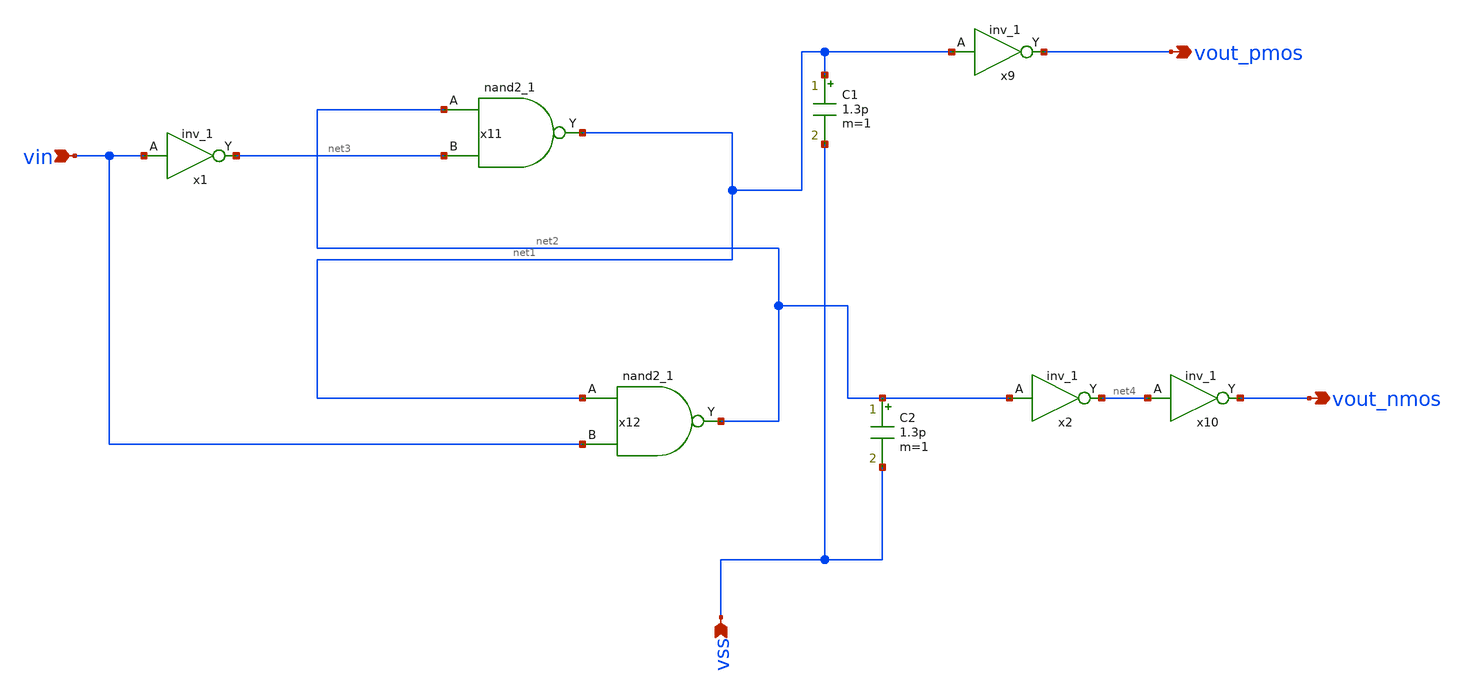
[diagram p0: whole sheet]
** sch_path: designs/libs/core_analog/Deadtime_Driver/op_Deadtime_Driver.sch
**.subckt op_Deadtime_Driver vin vss vout_pmos vout_nmos
*.ipin vin
*.ipin vss
*.opin vout_pmos
*.opin vout_nmos
C1 net1 vss 1.3p m=1
C2 net2 vss 1.3p m=1
x1 vin VSSd VDDd VSSd VDDd net3 gf180mcu_fd_sc_mcu9t5v0__inv_1
x2 net2 VSSd VDDd VSSd VDDd net4 gf180mcu_fd_sc_mcu9t5v0__inv_1
x9 net1 VSSd VDDd VSSd VDDd vout_pmos gf180mcu_fd_sc_mcu9t5v0__inv_1
x10 net4 VSSd VDDd VSSd VDDd vout_nmos gf180mcu_fd_sc_mcu9t5v0__inv_1
x11 net2 net3 VSSd VDDd VSSd VDDd net1 gf180mcu_fd_sc_mcu9t5v0__nand2_1
x12 net1 vin VSSd VDDd VSSd VDDd net2 gf180mcu_fd_sc_mcu9t5v0__nand2_1
**** begin user architecture code

.include $::180MCU_MODELS/design.ngspice
.include /foss/pdks/gf180mcuD/libs.ref/gf180mcu_fd_sc_mcu9t5v0/spice/gf180mcu_fd_sc_mcu9t5v0.spice
.lib $::180MCU_MODELS/sm141064.ngspice typical




.global VDDd VSSd
.control
save all
**Frequency & time settings
let fsig = 900k
let tper=1/fsig
let tfr = 0.01*tper
let ton = 0.5*tper-2*tfr

let tstop = 4 * tper
let tstep = 0.001*tper


**voltages
alter @Vin[PULSE] = [ 0 2.3 0 $&tfr $&tfr $&ton $&tper 3 ]
alter @Vin[DC] = 0
*alter @Vin[SIN] = [ 1.7 1.5 $&fsig 0 0 ]

**simulation
OP
*show all > op.log
show all

tran $&tstep $&tstop

**Rise and Fall time for delay checking
meas tran trise_p TRIG v(pmos) VAL=0.66 RISE=3 TARG v(pmos) VAL=3.0 RISE=3
meas tran trise_n TRIG v(nmos) VAL=0.66 RISE=3 TARG v(nmos) VAL=3.0 RISE=3

meas tran tfall_p TRIG v(pmos) VAL=3.0 FALL=2 TARG v(pmos) VAL=0.66 FALL=2
meas tran tfall_n TRIG v(nmos) VAL=3.0 FALL=2 TARG v(nmos) VAL=0.66 FALL=2

plot nmos pmos

**Buffer overshoot checker

meas tran nmos_min MIN v(nmos)
meas tran nmos_max MAX v(nmos)

**AC simulation
AC dec 100 1 10e6
*plot db(v(nmos)) db(v(pmos))
*plot 180*cph(v(nmos))/pi 180*cph(v(pmos))/pi

write Deadtime_Driver_tb.raw
.endc


**** end user architecture code
**.ends
.end
